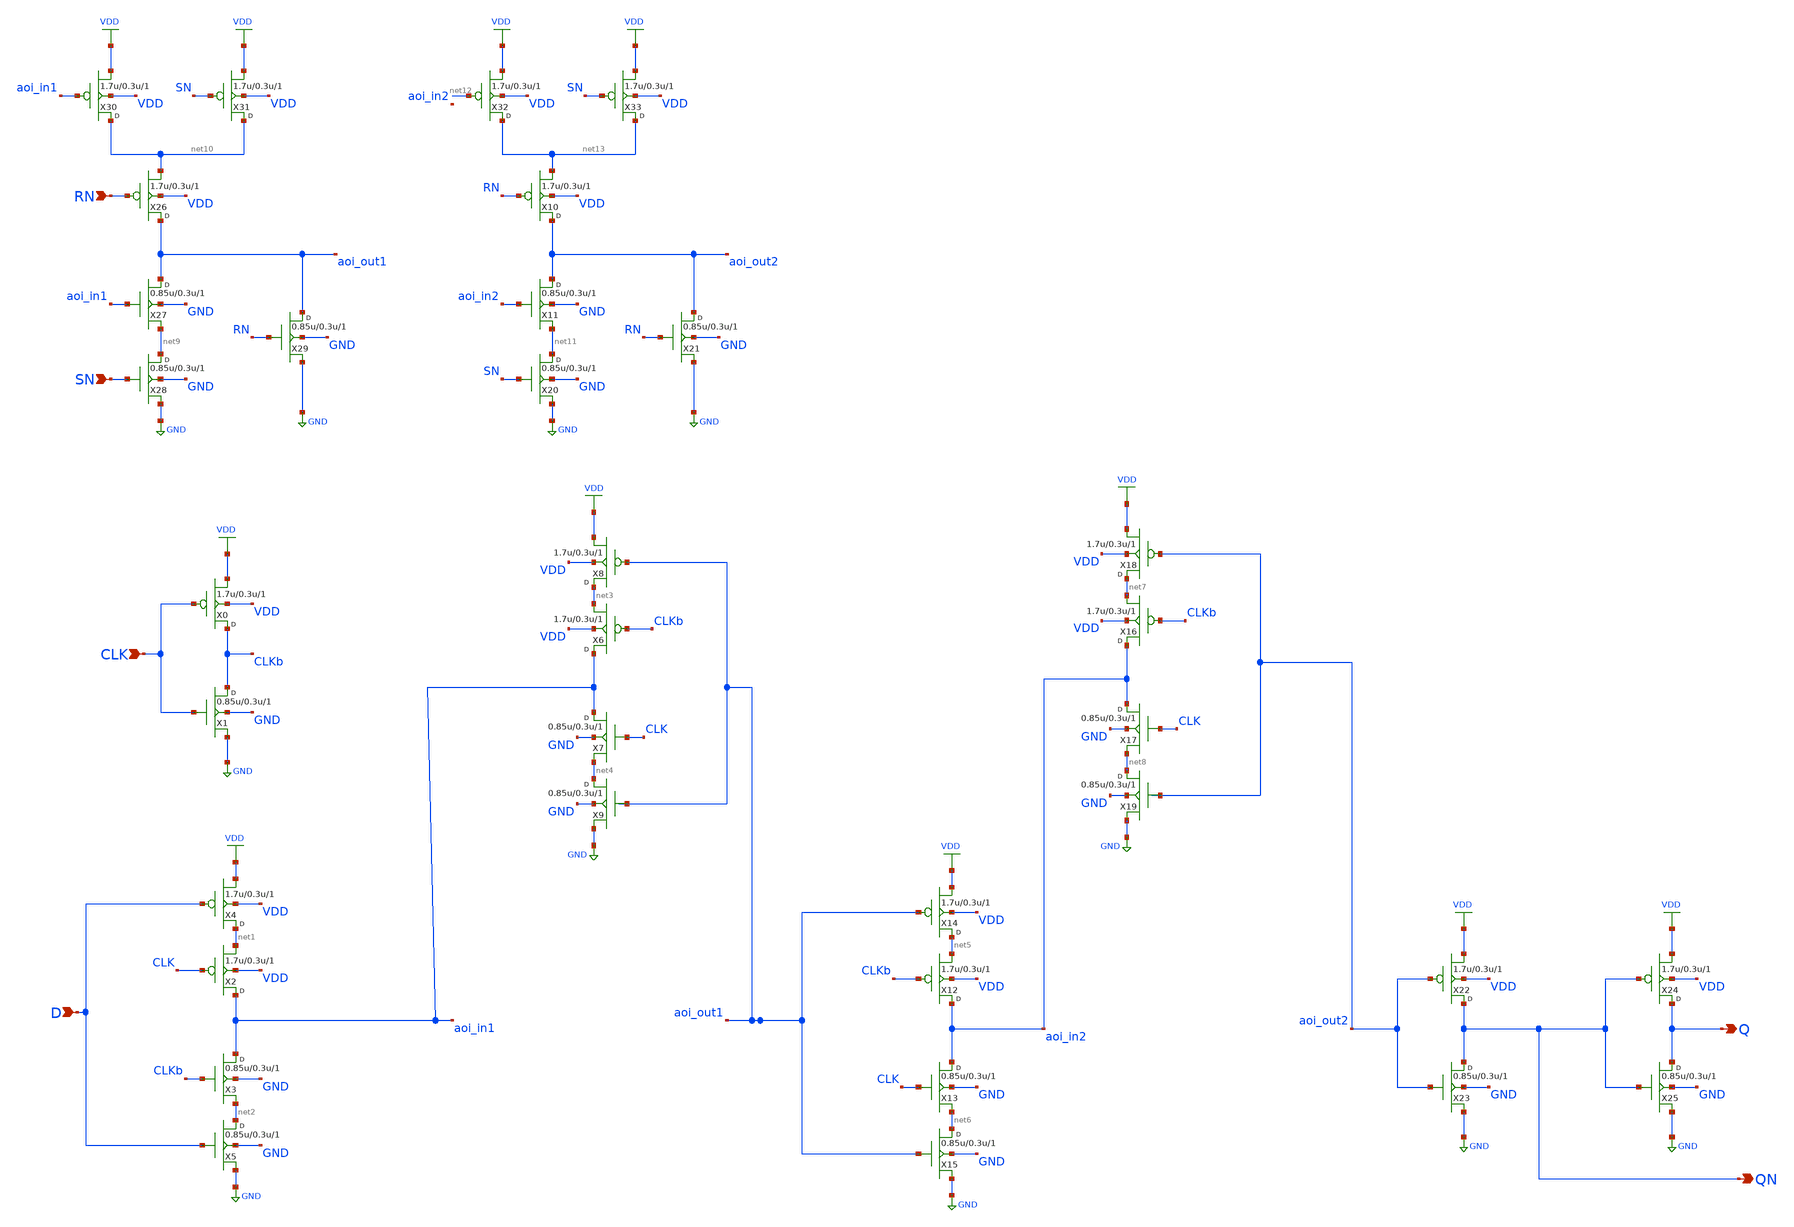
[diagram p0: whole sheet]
** sch_path: gf180mcu_osu_sc_gp12t3v3/cells/dffsr/gf180mcu_osu_sc_gp12t3v3__dffsr_1.sch
**.subckt gf180mcu_osu_sc_gp12t3v3__dffsr_1 CLK D Q QN SN RN
*.ipin CLK
*.ipin D
*.opin Q
*.opin QN
*.ipin SN
*.ipin RN
X0 CLKb CLK VDD VDD pfet_03p3 w=1.7u l=0.3u m=1
X1 CLKb CLK GND GND nfet_03p3 w=0.85u l=0.3u m=1
X2 aoi_in1 CLK net1 VDD pfet_03p3 w=1.7u l=0.3u m=1
X3 aoi_in1 CLKb net2 GND nfet_03p3 w=0.85u l=0.3u m=1
X4 net1 D VDD VDD pfet_03p3 w=1.7u l=0.3u m=1
X5 net2 D GND GND nfet_03p3 w=0.85u l=0.3u m=1
X6 aoi_in1 CLKb net3 VDD pfet_03p3 w=1.7u l=0.3u m=1
X7 aoi_in1 CLK net4 GND nfet_03p3 w=0.85u l=0.3u m=1
X8 net3 aoi_out1 VDD VDD pfet_03p3 w=1.7u l=0.3u m=1
X9 net4 aoi_out1 GND GND nfet_03p3 w=0.85u l=0.3u m=1
X12 aoi_in2 CLKb net5 VDD pfet_03p3 w=1.7u l=0.3u m=1
X13 aoi_in2 CLK net6 GND nfet_03p3 w=0.85u l=0.3u m=1
X14 net5 aoi_out1 VDD VDD pfet_03p3 w=1.7u l=0.3u m=1
X15 net6 aoi_out1 GND GND nfet_03p3 w=0.85u l=0.3u m=1
X16 aoi_in2 CLKb net7 VDD pfet_03p3 w=1.7u l=0.3u m=1
X17 aoi_in2 CLK net8 GND nfet_03p3 w=0.85u l=0.3u m=1
X18 net7 aoi_out2 VDD VDD pfet_03p3 w=1.7u l=0.3u m=1
X19 net8 aoi_out2 GND GND nfet_03p3 w=0.85u l=0.3u m=1
X22 QN aoi_out2 VDD VDD pfet_03p3 w=1.7u l=0.3u m=1
X23 QN aoi_out2 GND GND nfet_03p3 w=0.85u l=0.3u m=1
X24 Q QN VDD VDD pfet_03p3 w=1.7u l=0.3u m=1
X25 Q QN GND GND nfet_03p3 w=0.85u l=0.3u m=1
X26 aoi_out1 RN net10 VDD pfet_03p3 w=1.7u l=0.3u m=1
X27 aoi_out1 aoi_in1 net9 GND nfet_03p3 w=0.85u l=0.3u m=1
X28 net9 SN GND GND nfet_03p3 w=0.85u l=0.3u m=1
X29 aoi_out1 RN GND GND nfet_03p3 w=0.85u l=0.3u m=1
X30 net10 aoi_in1 VDD VDD pfet_03p3 w=1.7u l=0.3u m=1
X31 net10 SN VDD VDD pfet_03p3 w=1.7u l=0.3u m=1
X10 aoi_out2 RN net13 VDD pfet_03p3 w=1.7u l=0.3u m=1
X11 aoi_out2 aoi_in2 net11 GND nfet_03p3 w=0.85u l=0.3u m=1
X20 net11 SN GND GND nfet_03p3 w=0.85u l=0.3u m=1
X21 aoi_out2 RN GND GND nfet_03p3 w=0.85u l=0.3u m=1
X32 net13 net12 VDD VDD pfet_03p3 w=1.7u l=0.3u m=1
X33 net13 SN VDD VDD pfet_03p3 w=1.7u l=0.3u m=1
**.ends
.GLOBAL VDD
.GLOBAL GND
.end
